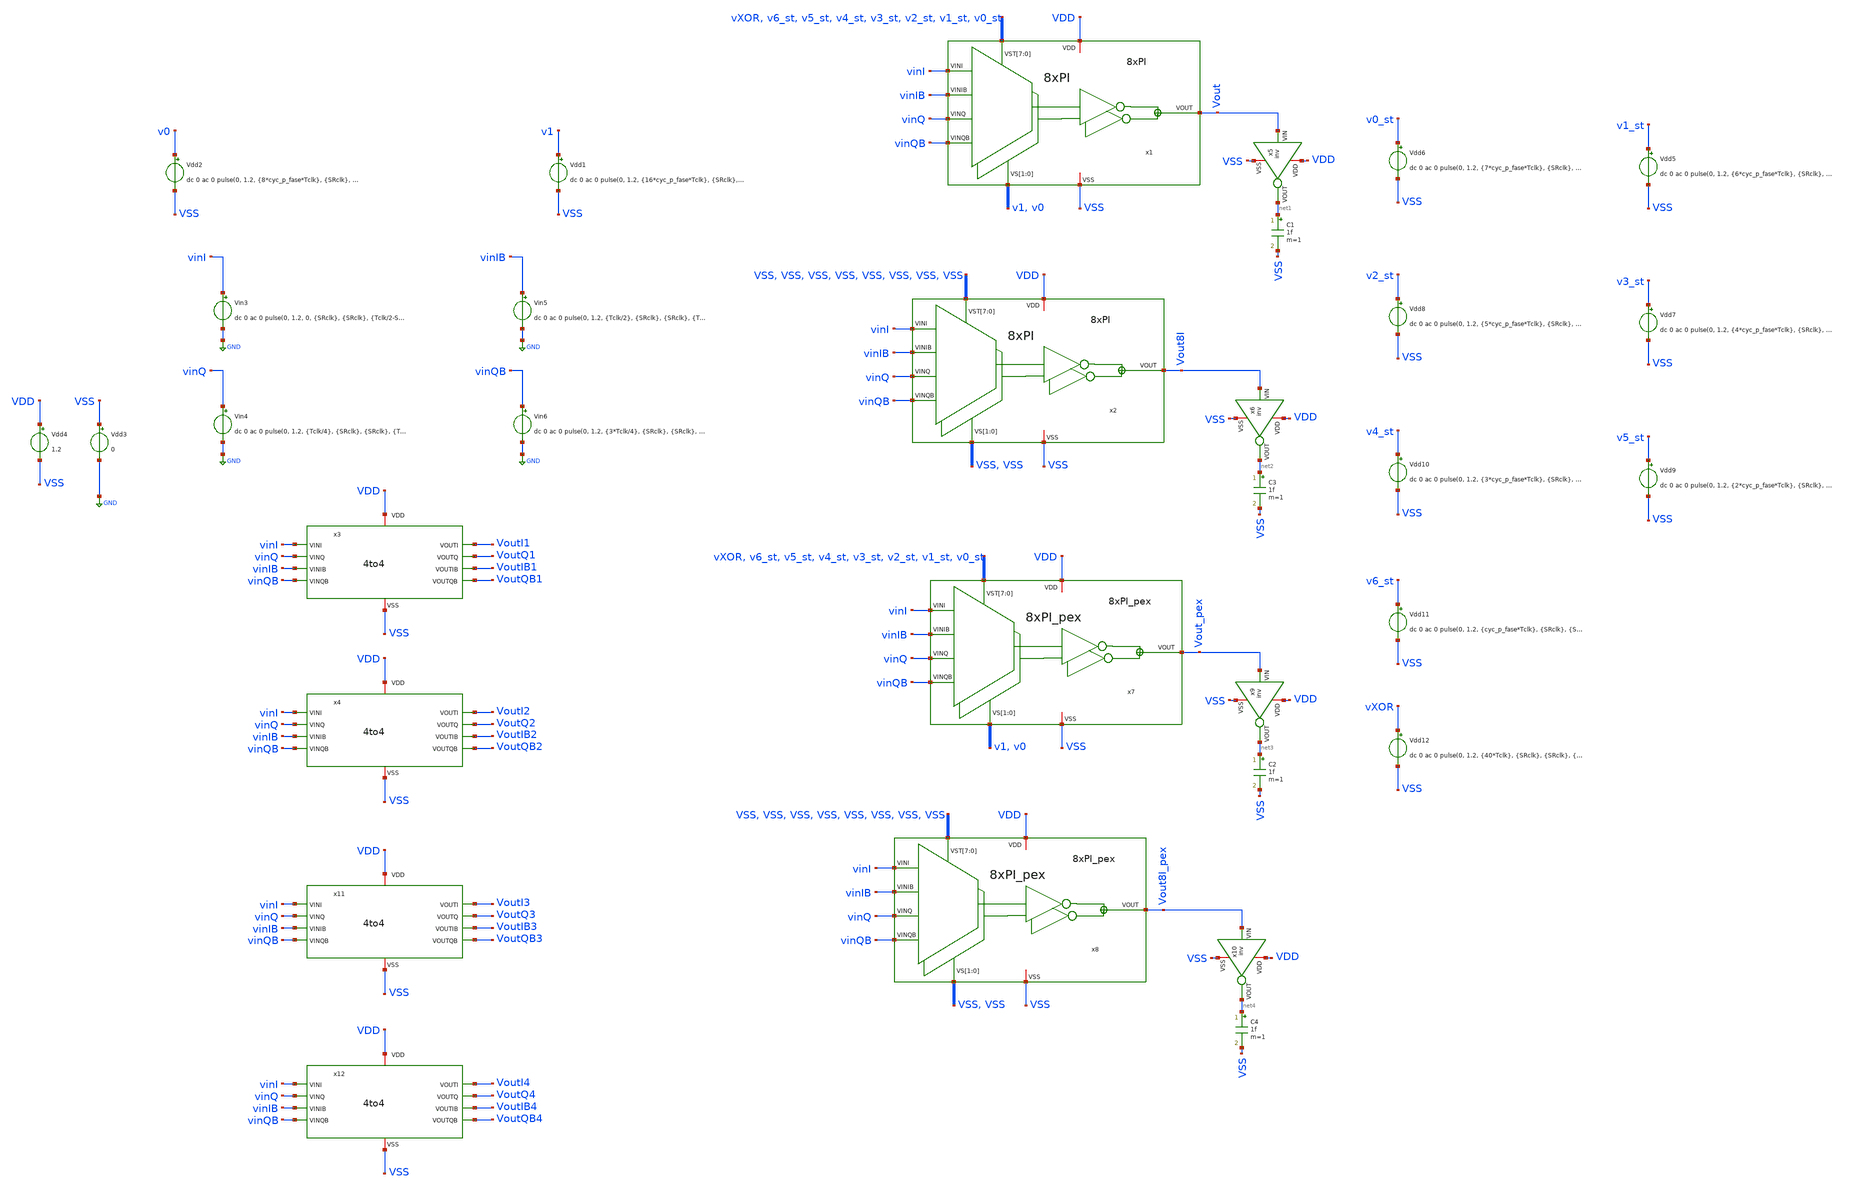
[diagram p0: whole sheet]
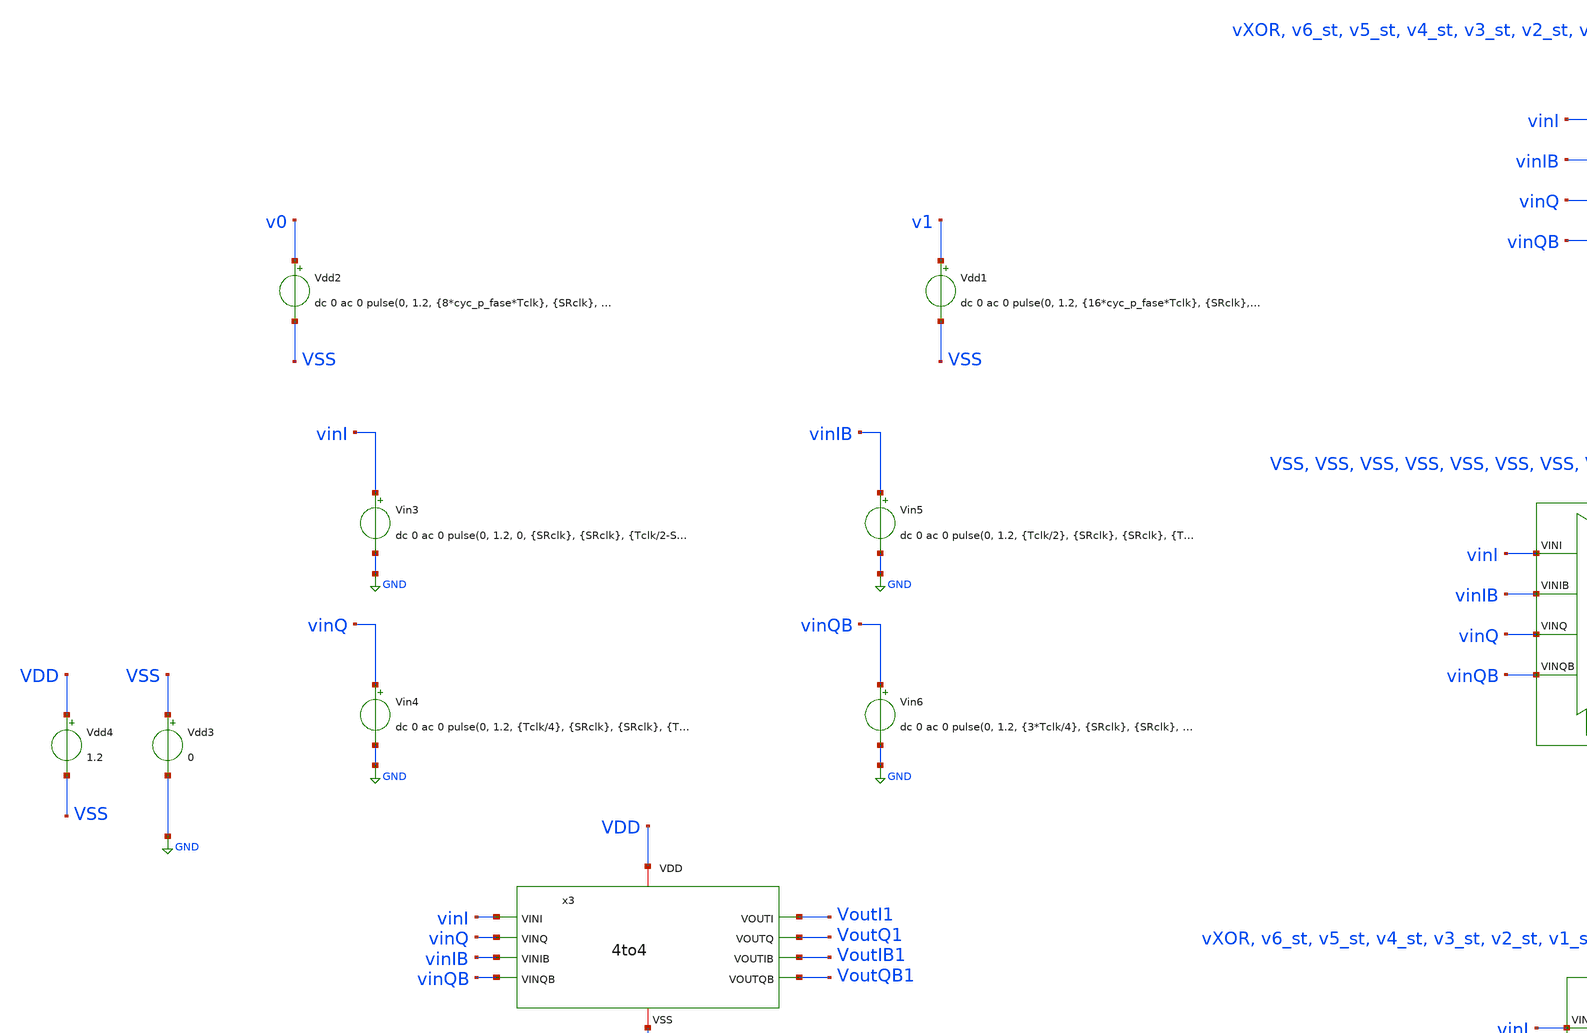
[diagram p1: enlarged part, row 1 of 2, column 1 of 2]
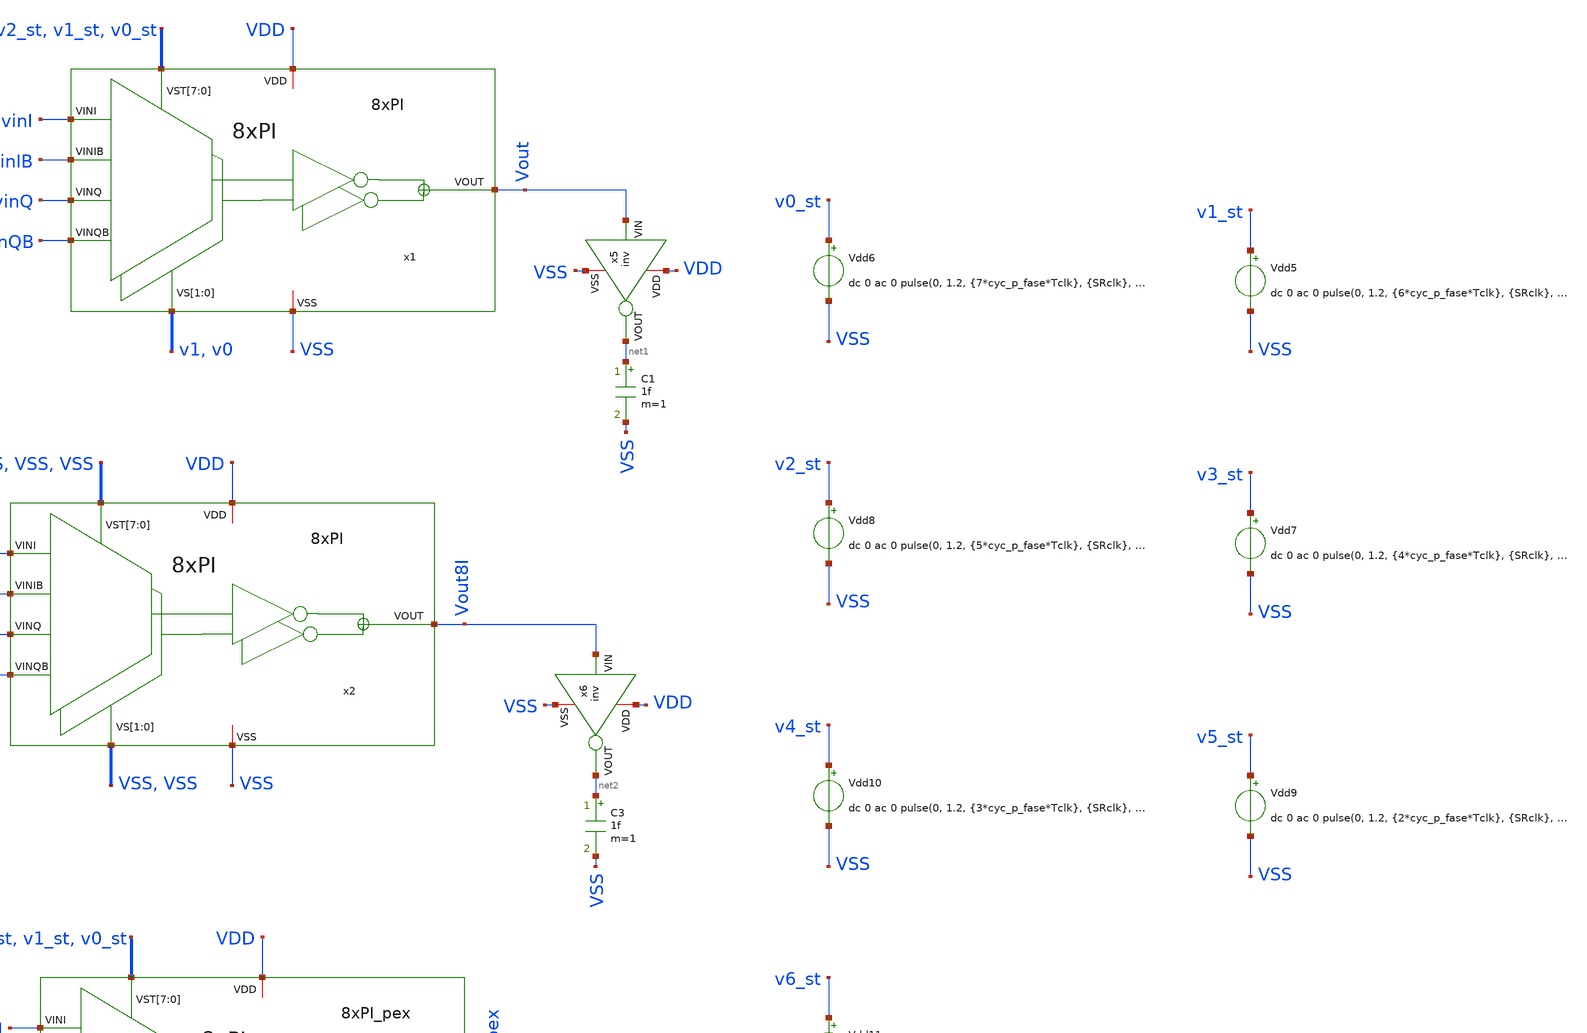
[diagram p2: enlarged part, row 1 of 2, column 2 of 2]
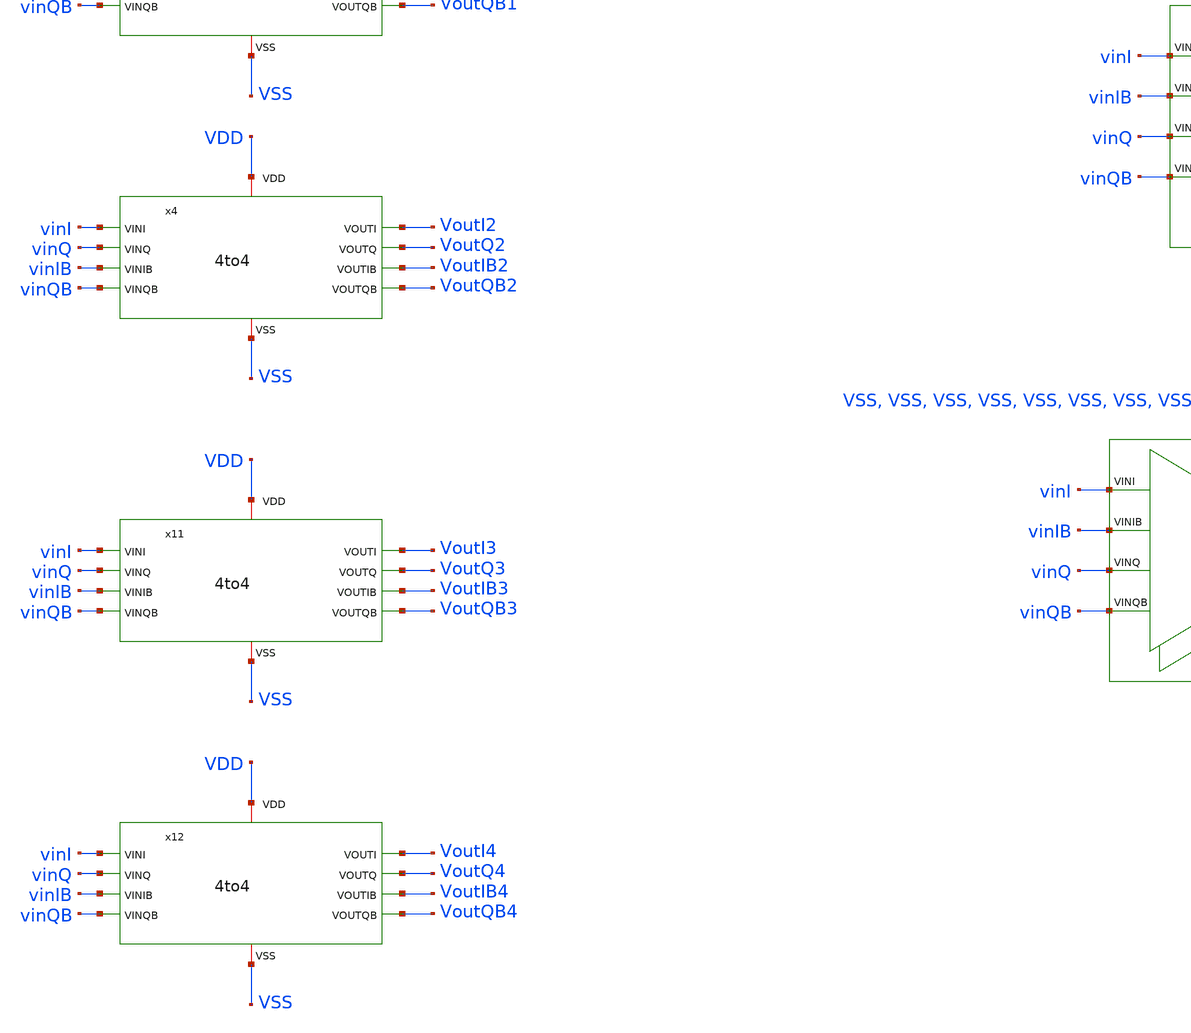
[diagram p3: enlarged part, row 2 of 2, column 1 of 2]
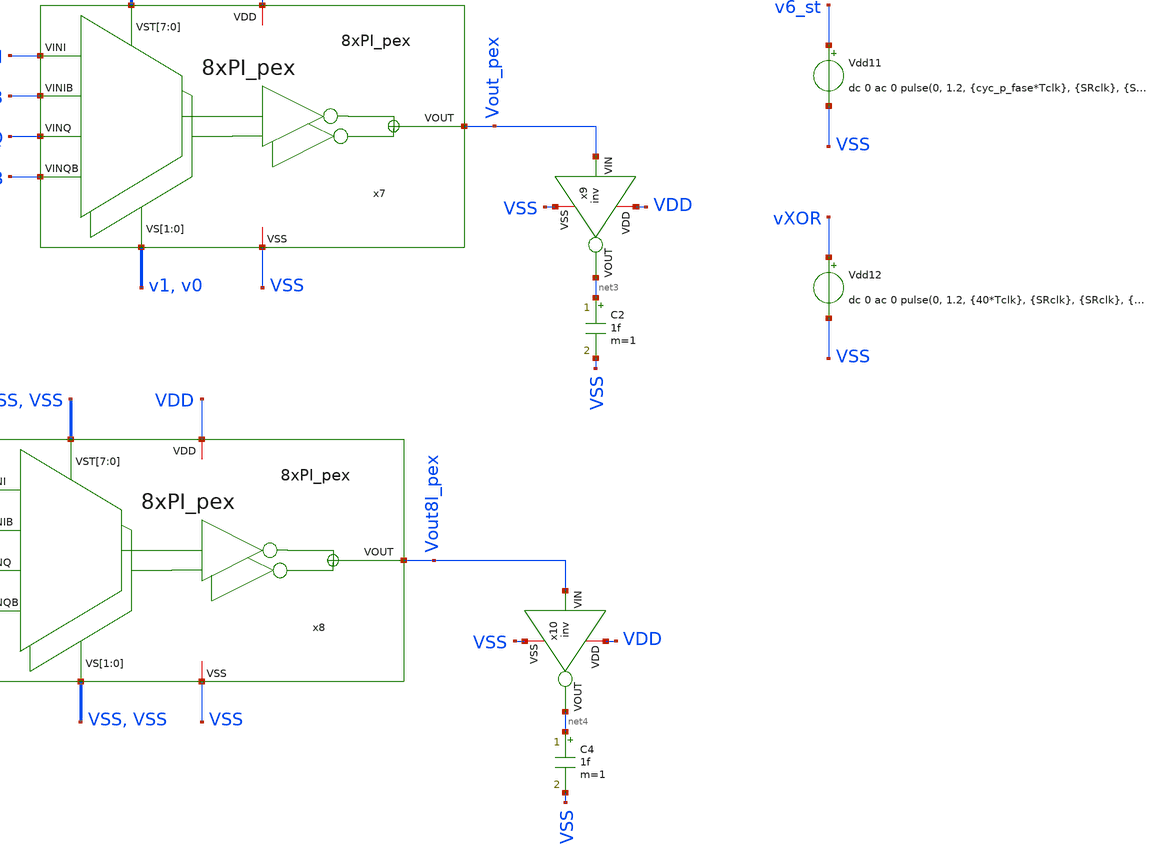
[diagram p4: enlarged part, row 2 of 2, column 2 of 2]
** sch_path: verification/testbenches/tb_8xPI_pex.sch
**.subckt tb_8xPI_pex
Vdd5 v1_st VSS dc 0 ac 0 pulse(0, 1.2, {6*cyc_p_fase*Tclk}, {SRclk}, {SRclk}, {2*cyc_p_fase*Tclk}, {8*cyc_p_fase*Tclk})
Vdd6 v0_st VSS dc 0 ac 0 pulse(0, 1.2, {7*cyc_p_fase*Tclk}, {SRclk}, {SRclk}, {cyc_p_fase*Tclk}, {8*cyc_p_fase*Tclk})
Vdd7 v3_st VSS dc 0 ac 0 pulse(0, 1.2, {4*cyc_p_fase*Tclk}, {SRclk}, {SRclk}, {4*cyc_p_fase*Tclk}, {8*cyc_p_fase*Tclk})
Vdd8 v2_st VSS dc 0 ac 0 pulse(0, 1.2, {5*cyc_p_fase*Tclk}, {SRclk}, {SRclk}, {3*cyc_p_fase*Tclk}, {8*cyc_p_fase*Tclk})
Vdd9 v5_st VSS dc 0 ac 0 pulse(0, 1.2, {2*cyc_p_fase*Tclk}, {SRclk}, {SRclk}, {6*cyc_p_fase*Tclk}, {8*cyc_p_fase*Tclk})
Vdd10 v4_st VSS dc 0 ac 0 pulse(0, 1.2, {3*cyc_p_fase*Tclk}, {SRclk}, {SRclk}, {5*cyc_p_fase*Tclk}, {8*cyc_p_fase*Tclk})
Vdd11 v6_st VSS dc 0 ac 0 pulse(0, 1.2, {cyc_p_fase*Tclk}, {SRclk}, {SRclk}, {7*cyc_p_fase*Tclk}, {8*cyc_p_fase*Tclk})
Vdd12 vXOR VSS dc 0 ac 0 pulse(0, 1.2, {40*Tclk}, {SRclk}, {SRclk}, {40*Tclk}, {80*Tclk})
Vin3 vinI GND dc 0 ac 0 pulse(0, 1.2, 0, {SRclk}, {SRclk}, {Tclk/2-SRclk}, {Tclk})
Vin4 vinQ GND dc 0 ac 0 pulse(0, 1.2, {Tclk/4}, {SRclk}, {SRclk}, {Tclk/2-SRclk}, {Tclk})
Vin5 vinIB GND dc 0 ac 0 pulse(0, 1.2, {Tclk/2}, {SRclk}, {SRclk}, {Tclk/2-SRclk}, {Tclk})
Vin6 vinQB GND dc 0 ac 0 pulse(0, 1.2, {3*Tclk/4}, {SRclk}, {SRclk}, {Tclk/2-SRclk}, {Tclk} )
Vdd4 VDD VSS 1.2
Vdd1 v1 VSS dc 0 ac 0 pulse(0, 1.2, {16*cyc_p_fase*Tclk}, {SRclk}, {SRclk}, {16cyc_p_fase*Tclk}, {32*cyc_p_fase*Tclk})
Vdd2 v0 VSS dc 0 ac 0 pulse(0, 1.2, {8*cyc_p_fase*Tclk}, {SRclk}, {SRclk}, {16*cyc_p_fase*Tclk}, {32*cyc_p_fase*Tclk})
Vdd3 VSS GND 0
x1 vinI vinIB vinQ vinQB v1 v0 vXOR v6_st v5_st v4_st v3_st v2_st v1_st v0_st Vout VDD VSS 8xPI
x2 vinI vinIB vinQ vinQB VSS VSS VSS VSS VSS VSS VSS VSS VSS VSS Vout8I VDD VSS 8xPI
x3 VDD vinI VoutI1 VoutQ1 vinQ vinIB VoutIB1 vinQB VoutQB1 VSS 4to4
x4 VDD vinI VoutI2 VoutQ2 vinQ vinIB VoutIB2 vinQB VoutQB2 VSS 4to4
x5 VDD net1 Vout VSS inv
C1 net1 VSS 1f m=1
x6 VDD net2 Vout8I VSS inv
C3 net2 VSS 1f m=1
x9 VDD net3 Vout_pex VSS inv
C2 net3 VSS 1f m=1
x10 VDD net4 Vout8I_pex VSS inv
C4 net4 VSS 1f m=1
x7 vinI vinIB vinQ vinQB v1 v0 vXOR v6_st v5_st v4_st v3_st v2_st v1_st v0_st Vout_pex VDD VSS
+ 8xPI_pex
x8 vinI vinIB vinQ vinQB VSS VSS VSS VSS VSS VSS VSS VSS VSS VSS Vout8I_pex VDD VSS 8xPI_pex
x11 VDD vinI VoutI3 VoutQ3 vinQ vinIB VoutIB3 vinQB VoutQB3 VSS 4to4
x12 VDD vinI VoutI4 VoutQ4 vinQ vinIB VoutIB4 vinQB VoutQB4 VSS 4to4
**** begin user architecture code



* Circuit Parameters
.param vdd = 1.2
.param vss = 0.0
.param a=0
.param b=0
.param c=0
.param d=1
.param Tclk = 1375p
.param cyc_p_fase = 5
.param SRclk = 50p
.options TEMP = 27.0
.options rshunt = 1e12

* Include Models
*.lib /opt/pdks/ihp-sg13g2/libs.tech/ngspice/models/cornerMOSlv.lib mos_tt
*.lib /opt/pdks/ihp-sg13g2/libs.tech/ngspice/models/cornerMOShv.lib mos_tt
*.lib /opt/pdks/ihp-sg13g2/libs.tech/ngspice/models/cornerHBT.lib hbt_typ
*.lib /opt/pdks/ihp-sg13g2/libs.tech/ngspice/models/cornerRES.lib res_typ
.inc /foss/designs/PhaseInterpolator/8xPI/8xPI_pex.spice
.lib cornerMOSlv.lib mos_tt

*         Initial Conditions
* tieh and tiel
.nodeset v(x1.x1[7].x1.tieh)={vdd} v(x1.x1[7].x1.tiel)=0 v(x1.x1[7].x3.tieh)={vdd} v(x1.x1[7].x3.tiel)=0
+ v(x1.x1[7].x5.tieh)={vdd} v(x1.x1[7].x5.tiel)=0
.nodeset v(x1.x1[6].x1.tieh)={vdd} v(x1.x1[6].x1.tiel)=0 v(x1.x1[6].x3.tieh)={vdd} v(x1.x1[6].x3.tiel)=0
+ v(x1.x1[6].x5.tieh)={vdd} v(x1.x1[6].x5.tiel)=0
.nodeset v(x1.x1[5].x1.tieh)={vdd} v(x1.x1[5].x1.tiel)=0 v(x1.x1[5].x3.tieh)={vdd} v(x1.x1[5].x3.tiel)=0
+ v(x1.x1[5].x5.tieh)={vdd} v(x1.x1[5].x5.tiel)=0
.nodeset v(x1.x1[4].x1.tieh)={vdd} v(x1.x1[4].x1.tiel)=0 v(x1.x1[4].x3.tieh)={vdd} v(x1.x1[4].x3.tiel)=0
+ v(x1.x1[4].x5.tieh)={vdd} v(x1.x1[4].x5.tiel)=0
.nodeset v(x1.x1[3].x1.tieh)={vdd} v(x1.x1[3].x1.tiel)=0 v(x1.x1[3].x3.tieh)={vdd} v(x1.x1[3].x3.tiel)=0
+ v(x1.x1[3].x5.tieh)={vdd} v(x1.x1[3].x5.tiel)=0
.nodeset v(x1.x1[2].x1.tieh)={vdd} v(x1.x1[2].x1.tiel)=0 v(x1.x1[2].x3.tieh)={vdd} v(x1.x1[2].x3.tiel)=0
+ v(x1.x1[2].x5.tieh)={vdd} v(x1.x1[2].x5.tiel)=0
.nodeset v(x1.x1[1].x1.tieh)={vdd} v(x1.x1[1].x1.tiel)=0 v(x1.x1[1].x3.tieh)={vdd} v(x1.x1[1].x3.tiel)=0
+ v(x1.x1[1].x5.tieh)={vdd} v(x1.x1[1].x5.tiel)=0
.nodeset v(x1.x1[0].x1.tieh)={vdd} v(x1.x1[0].x1.tiel)=0 v(x1.x1[0].x3.tieh)={vdd} v(x1.x1[0].x3.tiel)=0
+ v(x1.x1[0].x5.tieh)={vdd} v(x1.x1[0].x5.tiel)=0
.nodeset v(x2.x1[7].x1.tieh)={vdd} v(x2.x1[7].x1.tiel)=0 v(x2.x1[7].x3.tieh)={vdd} v(x2.x1[7].x3.tiel)=0
+ v(x2.x1[7].x5.tieh)={vdd} v(x2.x1[7].x5.tiel)=0
.nodeset v(x2.x1[6].x1.tieh)={vdd} v(x2.x1[6].x1.tiel)=0 v(x2.x1[6].x3.tieh)={vdd} v(x2.x1[6].x3.tiel)=0
+ v(x2.x1[6].x5.tieh)={vdd} v(x2.x1[6].x5.tiel)=0
.nodeset v(x2.x1[5].x1.tieh)={vdd} v(x2.x1[5].x1.tiel)=0 v(x2.x1[5].x3.tieh)={vdd} v(x2.x1[5].x3.tiel)=0
+ v(x2.x1[5].x5.tieh)={vdd} v(x2.x1[5].x5.tiel)=0
.nodeset v(x2.x1[4].x1.tieh)={vdd} v(x2.x1[4].x1.tiel)=0 v(x2.x1[4].x3.tieh)={vdd} v(x2.x1[4].x3.tiel)=0
+ v(x2.x1[4].x5.tieh)={vdd} v(x2.x1[4].x5.tiel)=0
.nodeset v(x2.x1[3].x1.tieh)={vdd} v(x2.x1[3].x1.tiel)=0 v(x2.x1[3].x3.tieh)={vdd} v(x2.x1[3].x3.tiel)=0
+ v(x2.x1[3].x5.tieh)={vdd} v(x2.x1[3].x5.tiel)=0
.nodeset v(x2.x1[2].x1.tieh)={vdd} v(x2.x1[2].x1.tiel)=0 v(x2.x1[2].x3.tieh)={vdd} v(x2.x1[2].x3.tiel)=0
+ v(x2.x1[2].x5.tieh)={vdd} v(x2.x1[2].x5.tiel)=0
.nodeset v(x2.x1[1].x1.tieh)={vdd} v(x2.x1[1].x1.tiel)=0 v(x2.x1[1].x3.tieh)={vdd} v(x2.x1[1].x3.tiel)=0
+ v(x2.x1[1].x5.tieh)={vdd} v(x2.x1[1].x5.tiel)=0
.nodeset v(x2.x1[0].x1.tieh)={vdd} v(x2.x1[0].x1.tiel)=0 v(x2.x1[0].x3.tieh)={vdd} v(x2.x1[0].x3.tiel)=0
+ v(x2.x1[0].x5.tieh)={vdd} v(x2.x1[0].x5.tiel)=0


* OP Parameters & Singals to save
.save V(Vout) V(Vout8I) V(Vout_pex) V(Vout8I_pex) V(vinI) V(vinIB) V(vinQ) V(vinQB) V(VoutI1) V(VoutI2) V(VoutQ1) V(VoutIB1) V(VoutQB1) V(x8.MUX_4_1_1.MUX_2_1_2.inv_PI_1.VOUT) V(x8.MUX_4_1_1.MUX_2_1_2.inv_PI_0.VOUT) V(x1.x1[0].x1.net3) V(x1.x1[0].x1.net4) V(x8.MUX_4_1_1.MUX_2_1_2.tg_custom_14.VSP.t1) V(x8.MUX_4_1_1.MUX_2_1_2.tg_custom_14.VSP.t2) V(x8.MUX_4_1_1.MUX_2_1_2.tg_custom_8.VSP)


*Simulations
.control
*set output_path = tb_linearity_8xpi/
	set ngdebug
	set verbose
	tran 5PS 18NS
	*setplot tran1
	*plot v0 v1+1.5 v0_st+3 v6_st+4.5 Vout+6 Vout8I+7.5 ylabel vout xlabel vin
	set filetype = ascii
        write tran_linearity_termoless_pex.raw
	*write {$output_path}tran_linearity_termoless.raw V(Vout) V(Vout8I) V(vinI) V(VoutI1) V(VoutI2) V(VoutQ1)
+ V(VoutIB1) V(VoutQB1)
.endc
.end

**** end user architecture code
**.ends
.GLOBAL GND
.end
